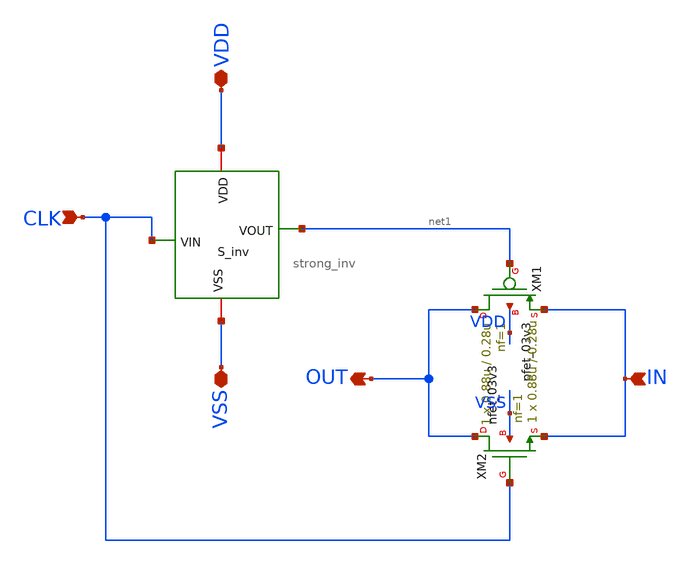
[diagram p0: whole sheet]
** sch_path: Clock_Generator_PAKISTAN_06/Schematics/strong_tg.sch
**.subckt strong_tg VDD VSS CLK IN OUT
*.iopin VDD
*.iopin VSS
*.ipin CLK
*.ipin IN
*.opin OUT
XM1 OUT net1 IN VDD pfet_03v3 L=0.28u W=0.88u nf=1 ad='int((nf+1)/2) * W/nf * 0.18u' as='int((nf+2)/2) * W/nf * 0.18u'
+ pd='2*int((nf+1)/2) * (W/nf + 0.18u)' ps='2*int((nf+2)/2) * (W/nf + 0.18u)' nrd='0.18u / W' nrs='0.18u / W'
+ sa=0 sb=0 sd=0 m=1
XM2 OUT CLK IN VSS nfet_03v3 L=0.28u W=0.88u nf=1 ad='int((nf+1)/2) * W/nf * 0.18u' as='int((nf+2)/2) * W/nf * 0.18u'
+ pd='2*int((nf+1)/2) * (W/nf + 0.18u)' ps='2*int((nf+2)/2) * (W/nf + 0.18u)' nrd='0.18u / W' nrs='0.18u / W'
+ sa=0 sb=0 sd=0 m=1
x1 VDD net1 CLK VSS strong_inv
**.ends
.end
